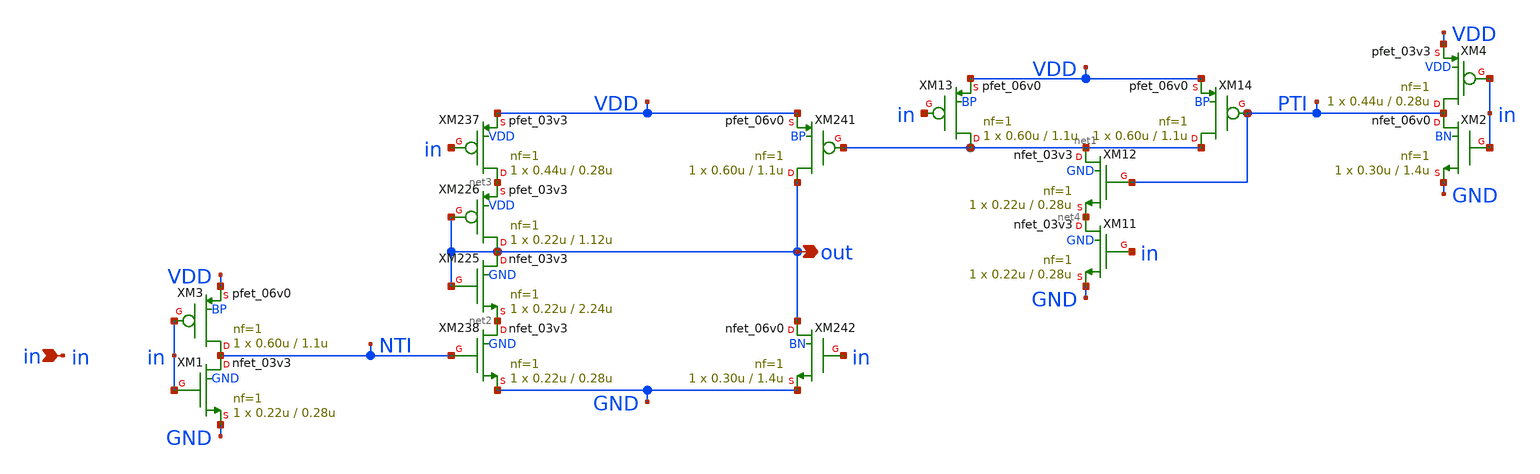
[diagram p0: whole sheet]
** sch_path: xschem_designs/cycle.sch
**.subckt cycle in out
*.ipin in
*.opin out
XM225 out out net2 GND nfet_03v3 L=2.24u W=0.22u nf=1 ad='int((nf+1)/2) * W/nf * 0.18u' as='int((nf+2)/2) * W/nf * 0.18u'
+ pd='2*int((nf+1)/2) * (W/nf + 0.18u)' ps='2*int((nf+2)/2) * (W/nf + 0.18u)' nrd='0.18u / W' nrs='0.18u / W'
+ sa=0 sb=0 sd=0 m=1 par=1
XM226 out out net3 VDD pfet_03v3 L=1.12u W=0.22u nf=1 ad='int((nf+1)/2) * W/nf * 0.18u' as='int((nf+2)/2) * W/nf * 0.18u'
+ pd='2*int((nf+1)/2) * (W/nf + 0.18u)' ps='2*int((nf+2)/2) * (W/nf + 0.18u)' nrd='0.18u / W' nrs='0.18u / W'
+ sa=0 sb=0 sd=0 m=1 par=1
XM237 net3 in VDD VDD pfet_03v3 L=0.28u W=0.44u nf=1 ad='int((nf+1)/2) * W/nf * 0.18u' as='int((nf+2)/2) * W/nf * 0.18u'
+ pd='2*int((nf+1)/2) * (W/nf + 0.18u)' ps='2*int((nf+2)/2) * (W/nf + 0.18u)' nrd='0.18u / W' nrs='0.18u / W'
+ sa=0 sb=0 sd=0 m=1 par=1
XM238 net2 NTI GND GND nfet_03v3 L=0.28u W=0.22u nf=1 ad='int((nf+1)/2) * W/nf * 0.18u' as='int((nf+2)/2) * W/nf * 0.18u'
+ pd='2*int((nf+1)/2) * (W/nf + 0.18u)' ps='2*int((nf+2)/2) * (W/nf + 0.18u)' nrd='0.18u / W' nrs='0.18u / W'
+ sa=0 sb=0 sd=0 m=1 par=1
XM241 out net1 VDD BP pfet_06v0 L=1.1u W=0.60u nf=1 ad='int((nf+1)/2) * W/nf * 0.18u' as='int((nf+2)/2) * W/nf * 0.18u'
+ pd='2*int((nf+1)/2) * (W/nf + 0.18u)' ps='2*int((nf+2)/2) * (W/nf + 0.18u)' nrd='0.18u / W' nrs='0.18u / W'
+ sa=0 sb=0 sd=0 m=1 par=1
XM242 out in GND BN nfet_06v0 L=1.4u W=0.30u nf=1 ad='int((nf+1)/2) * W/nf * 0.18u' as='int((nf+2)/2) * W/nf * 0.18u'
+ pd='2*int((nf+1)/2) * (W/nf + 0.18u)' ps='2*int((nf+2)/2) * (W/nf + 0.18u)' nrd='0.18u / W' nrs='0.18u / W'
+ sa=0 sb=0 sd=0 m=1 par=1
XM1 NTI in GND GND nfet_03v3 L=0.28u W=0.22u nf=1 ad='int((nf+1)/2) * W/nf * 0.18u' as='int((nf+2)/2) * W/nf * 0.18u'
+ pd='2*int((nf+1)/2) * (W/nf + 0.18u)' ps='2*int((nf+2)/2) * (W/nf + 0.18u)' nrd='0.18u / W' nrs='0.18u / W'
+ sa=0 sb=0 sd=0 m=1 par=1
XM2 PTI in GND BN nfet_06v0 L=1.4u W=0.30u nf=1 ad='int((nf+1)/2) * W/nf * 0.18u' as='int((nf+2)/2) * W/nf * 0.18u'
+ pd='2*int((nf+1)/2) * (W/nf + 0.18u)' ps='2*int((nf+2)/2) * (W/nf + 0.18u)' nrd='0.18u / W' nrs='0.18u / W'
+ sa=0 sb=0 sd=0 m=1 par=1
XM3 NTI in VDD BP pfet_06v0 L=1.1u W=0.60u nf=1 ad='int((nf+1)/2) * W/nf * 0.18u' as='int((nf+2)/2) * W/nf * 0.18u'
+ pd='2*int((nf+1)/2) * (W/nf + 0.18u)' ps='2*int((nf+2)/2) * (W/nf + 0.18u)' nrd='0.18u / W' nrs='0.18u / W'
+ sa=0 sb=0 sd=0 m=1 par=1
XM4 PTI in VDD VDD pfet_03v3 L=0.28u W=0.44u nf=1 ad='int((nf+1)/2) * W/nf * 0.18u' as='int((nf+2)/2) * W/nf * 0.18u'
+ pd='2*int((nf+1)/2) * (W/nf + 0.18u)' ps='2*int((nf+2)/2) * (W/nf + 0.18u)' nrd='0.18u / W' nrs='0.18u / W'
+ sa=0 sb=0 sd=0 m=1 par=1
XM11 net4 in GND GND nfet_03v3 L=0.28u W=0.22u nf=1 ad='int((nf+1)/2) * W/nf * 0.18u' as='int((nf+2)/2) * W/nf * 0.18u'
+ pd='2*int((nf+1)/2) * (W/nf + 0.18u)' ps='2*int((nf+2)/2) * (W/nf + 0.18u)' nrd='0.18u / W' nrs='0.18u / W'
+ sa=0 sb=0 sd=0 m=1 par=1
XM12 net1 PTI net4 GND nfet_03v3 L=0.28u W=0.22u nf=1 ad='int((nf+1)/2) * W/nf * 0.18u' as='int((nf+2)/2) * W/nf * 0.18u'
+ pd='2*int((nf+1)/2) * (W/nf + 0.18u)' ps='2*int((nf+2)/2) * (W/nf + 0.18u)' nrd='0.18u / W' nrs='0.18u / W'
+ sa=0 sb=0 sd=0 m=1 par=1
XM13 net1 in VDD BP pfet_06v0 L=1.1u W=0.60u nf=1 ad='int((nf+1)/2) * W/nf * 0.18u' as='int((nf+2)/2) * W/nf * 0.18u'
+ pd='2*int((nf+1)/2) * (W/nf + 0.18u)' ps='2*int((nf+2)/2) * (W/nf + 0.18u)' nrd='0.18u / W' nrs='0.18u / W'
+ sa=0 sb=0 sd=0 m=1 par=1
XM14 net1 PTI VDD BP pfet_06v0 L=1.1u W=0.60u nf=1 ad='int((nf+1)/2) * W/nf * 0.18u' as='int((nf+2)/2) * W/nf * 0.18u'
+ pd='2*int((nf+1)/2) * (W/nf + 0.18u)' ps='2*int((nf+2)/2) * (W/nf + 0.18u)' nrd='0.18u / W' nrs='0.18u / W'
+ sa=0 sb=0 sd=0 m=1 par=1
**.ends
.end
